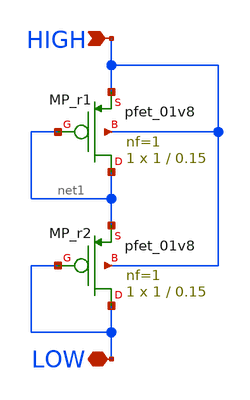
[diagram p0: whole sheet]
** sch_path: schem/symbol_repo/sym_pseudo_res.sch
**.subckt sym_pseudo_res LOW HIGH
*.iopin LOW
*.ipin HIGH
XMP_r1 net1 net1 HIGH HIGH sky130_fd_pr__pfet_01v8 L=0.15 W=1 nf=1 ad='int((1 + 1)/2) * 1 / 1 * 0.29'
+ as='int((1 + 2)/2) * 1 / 1 * 0.29' pd='2*int((1 + 1)/2) * (1 / 1 + 0.29)' ps='2*int((1 + 2)/2) * (1 / 1 + 0.29)'
+ nrd='0.29 / 1 ' nrs='0.29 / 1 ' sa=0 sb=0 sd=0 mult=1 m=1
XMP_r2 LOW LOW net1 HIGH sky130_fd_pr__pfet_01v8 L=0.15 W=1 nf=1 ad='int((1 + 1)/2) * 1 / 1 * 0.29' as='int((1 + 2)/2) * 1 / 1 * 0.29'
+ pd='2*int((1 + 1)/2) * (1 / 1 + 0.29)' ps='2*int((1 + 2)/2) * (1 / 1 + 0.29)' nrd='0.29 / 1 ' nrs='0.29 / 1 '
+ sa=0 sb=0 sd=0 mult=1 m=1
**.ends
.end
